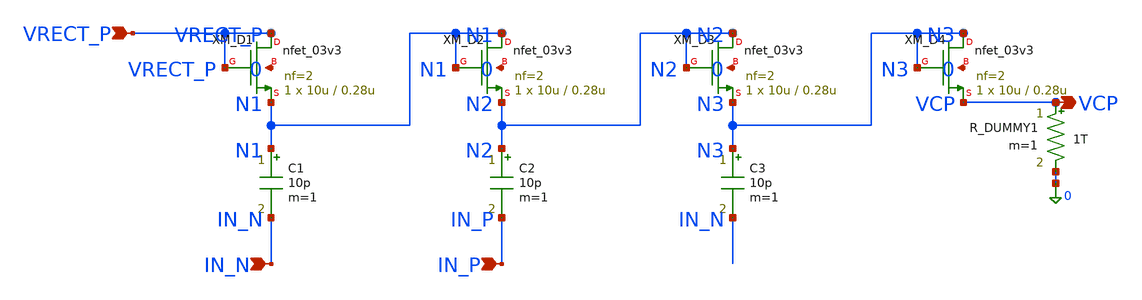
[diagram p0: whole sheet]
** sch_path: modules/PandaChip/designs/iris-harvester/exp/charge_pump.sch
**.subckt charge_pump VRECT_P IN_N IN_P VCP
*.ipin VRECT_P
*.ipin IN_N
*.ipin IN_P
*.opin VCP
XM_D1 VRECT_P VRECT_P N1 0 nfet_03v3 L=0.28u W=10u nf=2 ad='int((nf+1)/2) * W/nf * 0.18u' as='int((nf+2)/2) * W/nf * 0.18u'
+ pd='2*int((nf+1)/2) * (W/nf + 0.18u)' ps='2*int((nf+2)/2) * (W/nf + 0.18u)' nrd='0.18u / W' nrs='0.18u / W'
+ sa=0 sb=0 sd=0 m=1
XM_D2 N1 N1 N2 0 nfet_03v3 L=0.28u W=10u nf=2 ad='int((nf+1)/2) * W/nf * 0.18u' as='int((nf+2)/2) * W/nf * 0.18u'
+ pd='2*int((nf+1)/2) * (W/nf + 0.18u)' ps='2*int((nf+2)/2) * (W/nf + 0.18u)' nrd='0.18u / W' nrs='0.18u / W'
+ sa=0 sb=0 sd=0 m=1
XM_D3 N2 N2 N3 0 nfet_03v3 L=0.28u W=10u nf=2 ad='int((nf+1)/2) * W/nf * 0.18u' as='int((nf+2)/2) * W/nf * 0.18u'
+ pd='2*int((nf+1)/2) * (W/nf + 0.18u)' ps='2*int((nf+2)/2) * (W/nf + 0.18u)' nrd='0.18u / W' nrs='0.18u / W'
+ sa=0 sb=0 sd=0 m=1
XM_D4 N3 N3 VCP 0 nfet_03v3 L=0.28u W=10u nf=2 ad='int((nf+1)/2) * W/nf * 0.18u' as='int((nf+2)/2) * W/nf * 0.18u'
+ pd='2*int((nf+1)/2) * (W/nf + 0.18u)' ps='2*int((nf+2)/2) * (W/nf + 0.18u)' nrd='0.18u / W' nrs='0.18u / W'
+ sa=0 sb=0 sd=0 m=1
C1 N1 IN_N 10p m=1
C2 N2 IN_P 10p m=1
C3 N3 IN_N 10p m=1
R_DUMMY1 VCP 0 1T m=1
**.ends
.end
